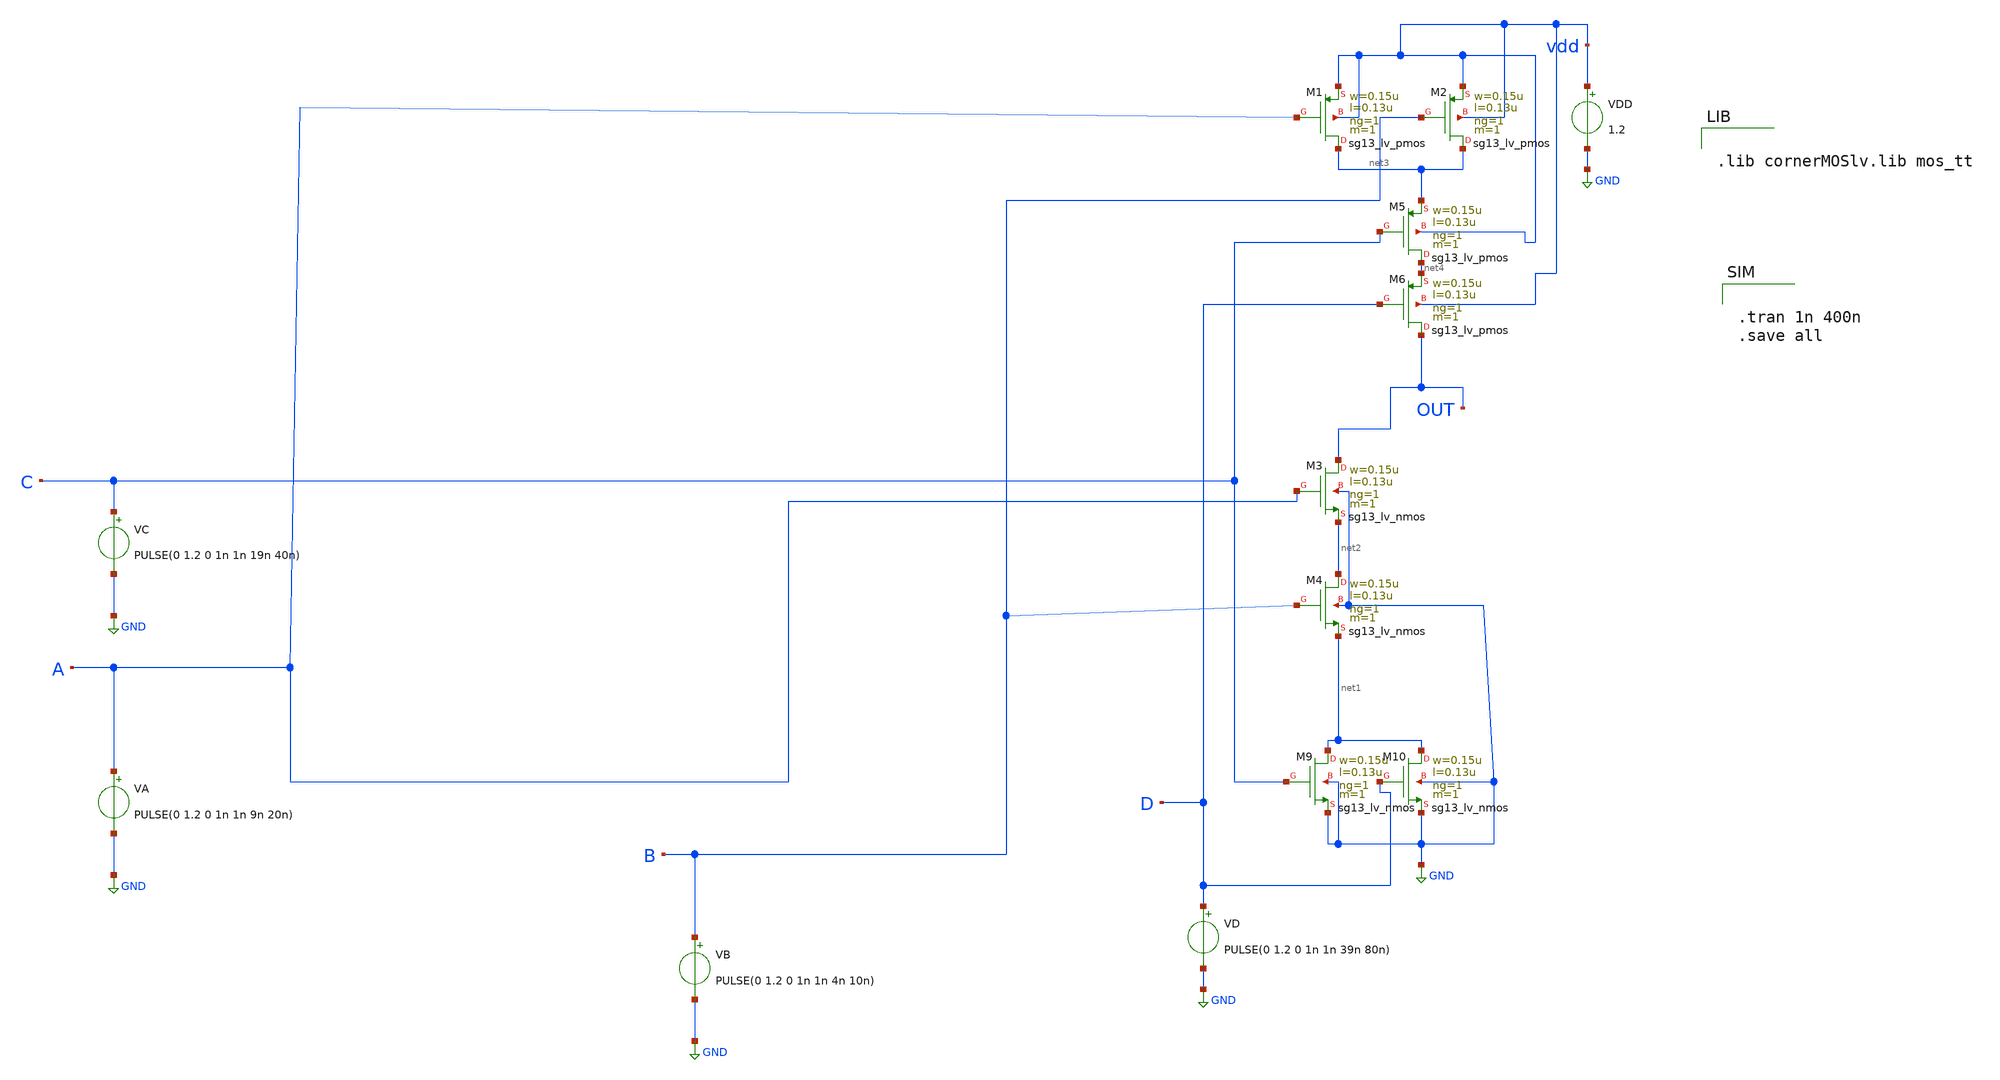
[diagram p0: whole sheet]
** sch_path: aoi211.sch
**.subckt aoi211
XM1 net3 A vdd vdd sg13_lv_pmos w=0.15u l=0.13u ng=1 m=1 mm_ok=1
XM2 net3 B vdd vdd sg13_lv_pmos w=0.15u l=0.13u ng=1 m=1 mm_ok=1
XM3 OUT A net2 GND sg13_lv_nmos w=0.15u l=0.13u ng=1 m=1 mm_ok=1
XM4 net2 B net1 GND sg13_lv_nmos w=0.15u l=0.13u ng=1 m=1 mm_ok=1
VDD vdd GND 1.2
VA A GND PULSE(0 1.2 0 1n 1n 9n 20n)
VB B GND PULSE(0 1.2 0 1n 1n 4n 10n)
XM5 net4 C net3 vdd sg13_lv_pmos w=0.15u l=0.13u ng=1 m=1 mm_ok=1
VC C GND PULSE(0 1.2 0 1n 1n 19n 40n)
VD D GND PULSE(0 1.2 0 1n 1n 39n 80n)
XM6 OUT D net4 vdd sg13_lv_pmos w=0.15u l=0.13u ng=1 m=1 mm_ok=1
XM9 net1 C GND GND sg13_lv_nmos w=0.15u l=0.13u ng=1 m=1 mm_ok=1
XM10 net1 D GND GND sg13_lv_nmos w=0.15u l=0.13u ng=1 m=1 mm_ok=1
**** begin user architecture code


.lib cornerMOSlv.lib mos_tt



.tran 1n 400n
.save all


**** end user architecture code
**.ends
.GLOBAL GND
.end
